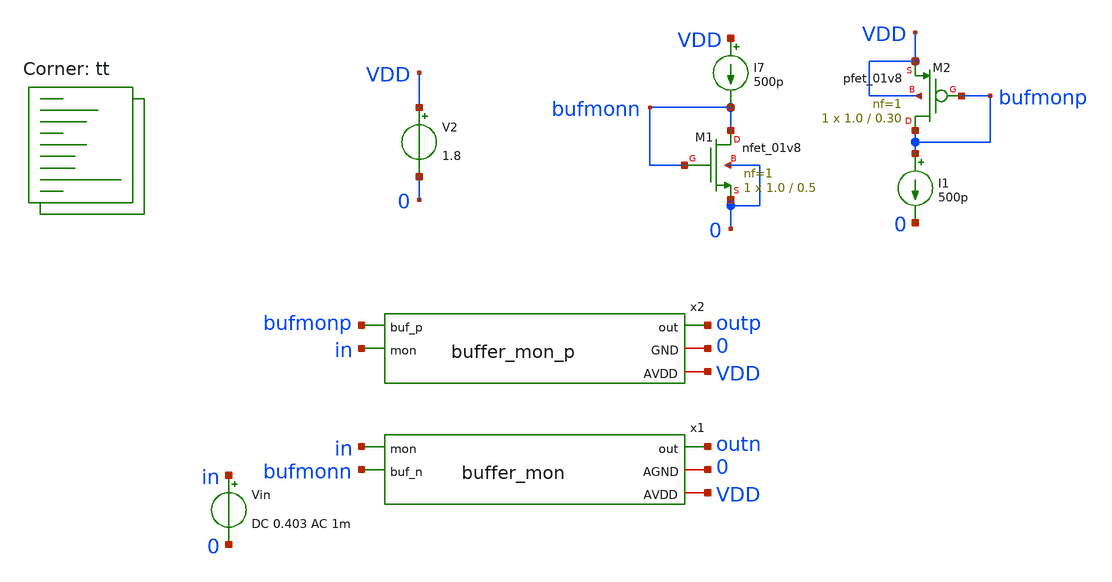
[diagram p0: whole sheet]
** sch_path: design/xschem/buffer_mon_tb.sch
**.subckt buffer_mon_tb
x1 outn in bufmonn 0 VDD buffer_mon
V2 VDD 0 1.8
I7 VDD bufmonn 500p
Vin in 0 DC 0.403 AC 1m
XM1 bufmonn bufmonn 0 0 sky130_fd_pr__nfet_01v8 L=0.5 W=1.0 nf=1 ad='int((nf+1)/2) * W/nf * 0.29' as='int((nf+2)/2) * W/nf * 0.29'
+ pd='2*int((nf+1)/2) * (W/nf + 0.29)' ps='2*int((nf+2)/2) * (W/nf + 0.29)' nrd='0.29 / W' nrs='0.29 / W'
+ sa=0 sb=0 sd=0 mult=1 m=1
x2 bufmonp outp in 0 VDD buffer_mon_p
I1 bufmonp 0 500p
XM2 bufmonp bufmonp VDD VDD sky130_fd_pr__pfet_01v8 L=0.30 W=1.0 nf=1 ad='int((nf+1)/2) * W/nf * 0.29'
+ as='int((nf+2)/2) * W/nf * 0.29' pd='2*int((nf+1)/2) * (W/nf + 0.29)' ps='2*int((nf+2)/2) * (W/nf + 0.29)'
+ nrd='0.29 / W' nrs='0.29 / W' sa=0 sb=0 sd=0 mult=1 m=1
**** begin user architecture code
.lib $::SKYWATER_MODELS/sky130.lib.spice tt



* ngspice commands
.save all

.save @m.x1.xm2.msky130_fd_pr__nfet_01v8[id]
.save @m.x1.xm2.msky130_fd_pr__nfet_01v8[gm]
.save @m.x1.xm3.msky130_fd_pr__nfet_01v8[id]
.save @m.x1.xm3.msky130_fd_pr__nfet_01v8[gm]
.save @m.x1.xm4.msky130_fd_pr__nfet_01v8[id]
.save @m.x1.xm4.msky130_fd_pr__nfet_01v8[gm]


.save @m.x1.xm1.msky130_fd_pr__pfet_01v8[id]
.save @m.x1.xm1.msky130_fd_pr__pfet_01v8[gm]
.save @m.x1.xm5.msky130_fd_pr__pfet_01v8[id]
.save @m.x1.xm5.msky130_fd_pr__pfet_01v8[gm]


.save @m.x2.xm4.msky130_fd_pr__nfet_01v8[id]
.save @m.x2.xm4.msky130_fd_pr__nfet_01v8[gm]
.save @m.x2.xm3.msky130_fd_pr__nfet_01v8[id]
.save @m.x2.xm3.msky130_fd_pr__nfet_01v8[gm]

.save @m.x2.xm1.msky130_fd_pr__pfet_01v8[id]
.save @m.x2.xm1.msky130_fd_pr__pfet_01v8[gm]
.save @m.x2.xm5.msky130_fd_pr__pfet_01v8[id]
.save @m.x2.xm5.msky130_fd_pr__pfet_01v8[gm]
.save @m.x2.xm2.msky130_fd_pr__pfet_01v8[id]
.save @m.x2.xm2.msky130_fd_pr__pfet_01v8[gm]


.control
op
write buffer_mon_tb.raw

dc vin 0 1.8 0.01
plot outn outp
*frequency sweep over Vin to find bandwith and gain
ac dec 10 1 1MEG
plot db(outp/in)
plot db(outn/in)
.endc



**** end user architecture code
**.ends

* expanding   symbol:  buffer_mon.sym # of pins=5
** sym_path: design/xschem/buffer_mon.sym
** sch_path: design/xschem/buffer_mon.sch
.subckt buffer_mon out mon buf_n AGND AVDD
*.iopin AGND
*.iopin AVDD
*.ipin buf_n
*.ipin mon
*.opin out
XM1 net2 net2 AVDD AVDD sky130_fd_pr__pfet_01v8 L=1.0 W=1.0 nf=1 ad='int((nf+1)/2) * W/nf * 0.29' as='int((nf+2)/2) * W/nf * 0.29'
+ pd='2*int((nf+1)/2) * (W/nf + 0.29)' ps='2*int((nf+2)/2) * (W/nf + 0.29)' nrd='0.29 / W' nrs='0.29 / W'
+ sa=0 sb=0 sd=0 mult=1 m=1
XM5 out net2 AVDD AVDD sky130_fd_pr__pfet_01v8 L=1.0 W=1.0 nf=1 ad='int((nf+1)/2) * W/nf * 0.29' as='int((nf+2)/2) * W/nf * 0.29'
+ pd='2*int((nf+1)/2) * (W/nf + 0.29)' ps='2*int((nf+2)/2) * (W/nf + 0.29)' nrd='0.29 / W' nrs='0.29 / W'
+ sa=0 sb=0 sd=0 mult=1 m=1
XM4 net1 buf_n AGND AGND sky130_fd_pr__nfet_01v8 L=0.5 W=1.0 nf=1 ad='int((nf+1)/2) * W/nf * 0.29' as='int((nf+2)/2) * W/nf * 0.29'
+ pd='2*int((nf+1)/2) * (W/nf + 0.29)' ps='2*int((nf+2)/2) * (W/nf + 0.29)' nrd='0.29 / W' nrs='0.29 / W'
+ sa=0 sb=0 sd=0 mult=1 m=1
XM2 net2 mon net1 AGND sky130_fd_pr__nfet_01v8 L=0.5 W=1.0 nf=1 ad='int((nf+1)/2) * W/nf * 0.29' as='int((nf+2)/2) * W/nf * 0.29'
+ pd='2*int((nf+1)/2) * (W/nf + 0.29)' ps='2*int((nf+2)/2) * (W/nf + 0.29)' nrd='0.29 / W' nrs='0.29 / W'
+ sa=0 sb=0 sd=0 mult=1 m=1
XM3 out out net1 AGND sky130_fd_pr__nfet_01v8 L=0.5 W=1.0 nf=1 ad='int((nf+1)/2) * W/nf * 0.29' as='int((nf+2)/2) * W/nf * 0.29'
+ pd='2*int((nf+1)/2) * (W/nf + 0.29)' ps='2*int((nf+2)/2) * (W/nf + 0.29)' nrd='0.29 / W' nrs='0.29 / W'
+ sa=0 sb=0 sd=0 mult=1 m=1
.ends


* expanding   symbol:  buffer_mon_p.sym # of pins=5
** sym_path: design/xschem/buffer_mon_p.sym
** sch_path: design/xschem/buffer_mon_p.sch
.subckt buffer_mon_p buf_p out mon GND AVDD
*.iopin GND
*.iopin AVDD
*.ipin buf_p
*.ipin mon
*.opin out
XM1 out out net2 AVDD sky130_fd_pr__pfet_01v8 L=0.5 W=1.0 nf=1 ad='int((nf+1)/2) * W/nf * 0.29' as='int((nf+2)/2) * W/nf * 0.29'
+ pd='2*int((nf+1)/2) * (W/nf + 0.29)' ps='2*int((nf+2)/2) * (W/nf + 0.29)' nrd='0.29 / W' nrs='0.29 / W'
+ sa=0 sb=0 sd=0 mult=1 m=1
XM5 net1 mon net2 AVDD sky130_fd_pr__pfet_01v8 L=0.5 W=1.0 nf=1 ad='int((nf+1)/2) * W/nf * 0.29' as='int((nf+2)/2) * W/nf * 0.29'
+ pd='2*int((nf+1)/2) * (W/nf + 0.29)' ps='2*int((nf+2)/2) * (W/nf + 0.29)' nrd='0.29 / W' nrs='0.29 / W'
+ sa=0 sb=0 sd=0 mult=1 m=1
XM2 net2 buf_p AVDD AVDD sky130_fd_pr__pfet_01v8 L=0.30 W=1.0 nf=1 ad='int((nf+1)/2) * W/nf * 0.29' as='int((nf+2)/2) * W/nf * 0.29'
+ pd='2*int((nf+1)/2) * (W/nf + 0.29)' ps='2*int((nf+2)/2) * (W/nf + 0.29)' nrd='0.29 / W' nrs='0.29 / W'
+ sa=0 sb=0 sd=0 mult=1 m=1
XM3 out net1 GND GND sky130_fd_pr__nfet_01v8 L=0.5 W=1.0 nf=1 ad='int((nf+1)/2) * W/nf * 0.29' as='int((nf+2)/2) * W/nf * 0.29'
+ pd='2*int((nf+1)/2) * (W/nf + 0.29)' ps='2*int((nf+2)/2) * (W/nf + 0.29)' nrd='0.29 / W' nrs='0.29 / W'
+ sa=0 sb=0 sd=0 mult=1 m=1
XM4 net1 net1 GND GND sky130_fd_pr__nfet_01v8 L=0.5 W=1.0 nf=1 ad='int((nf+1)/2) * W/nf * 0.29' as='int((nf+2)/2) * W/nf * 0.29'
+ pd='2*int((nf+1)/2) * (W/nf + 0.29)' ps='2*int((nf+2)/2) * (W/nf + 0.29)' nrd='0.29 / W' nrs='0.29 / W'
+ sa=0 sb=0 sd=0 mult=1 m=1
.ends

.end
